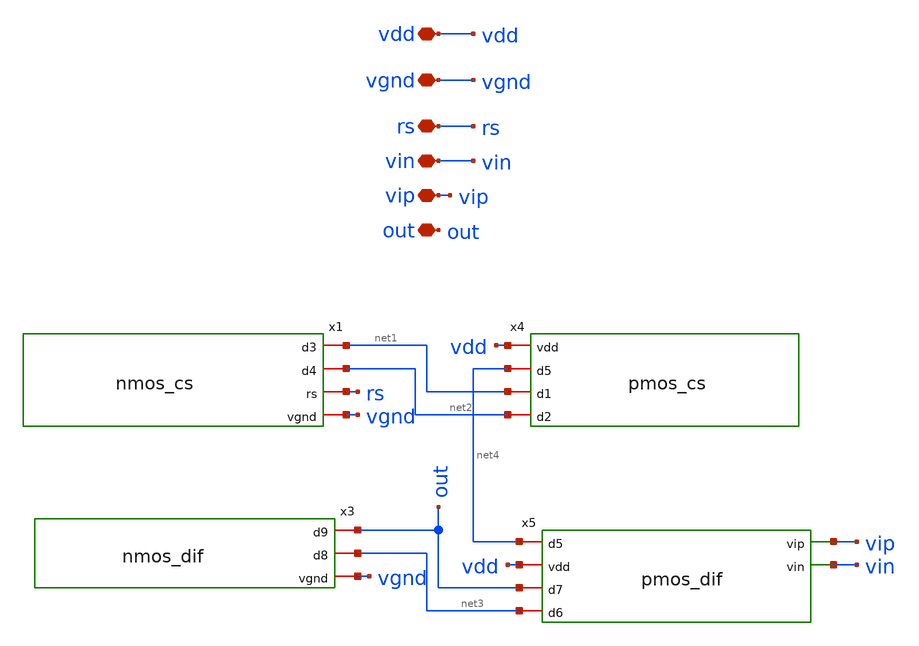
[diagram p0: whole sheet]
** sch_path: mag/opamp.sch
**.subckt opamp vdd vgnd rs vin vip out
*.iopin vdd
*.iopin vgnd
*.iopin rs
*.iopin vin
*.iopin vip
*.iopin out
x3 out net3 vgnd nmos_dif
x4 vdd net4 net1 net2 pmos_cs
x5 net4 vdd vip vin out net3 pmos_dif
x1 net1 net2 rs vgnd nmos_cs
**.ends
.end
